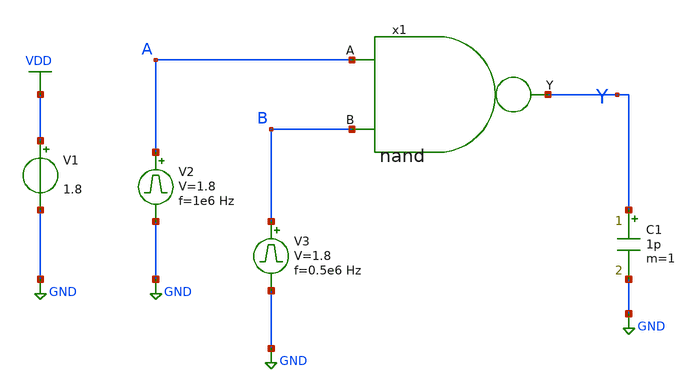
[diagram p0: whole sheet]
** sch_path: library/xschem/nand_tb.sch
**.subckt nand_tb
V1 VDD GND 1.8
V2 A GND pulse 0 1.8 '0.495/ 1e6 ' '0.01/1e6 ' '0.01/1e6 ' '0.49/1e6 ' '1/1e6 '
C1 Y GND 1p m=1
x1 A Y B nand
V3 B GND pulse 0 1.8 '0.495/ 0.5e6 ' '0.01/0.5e6 ' '0.01/0.5e6 ' '0.49/0.5e6 ' '1/0.5e6 '
**** begin user architecture code


.control
save all
tran 1n 2u
plot V(A) V(B)+2 V(Y)+4
.endc



** opencircuitdesign pdks install
.lib $::SKYWATER_MODELS/sky130.lib.spice tt


**** end user architecture code
**.ends

* expanding   symbol:  nand.sym # of pins=3
** sym_path: library/xschem/nand.sym
** sch_path: library/xschem/nand.sch
.subckt nand A Y B
*.ipin A
*.opin Y
*.ipin B
XM1 Y A net1 GND sky130_fd_pr__nfet_01v8 L=0.15 W=0.5 nf=1 ad='int((nf+1)/2) * W/nf * 0.29' as='int((nf+2)/2) * W/nf * 0.29'
+ pd='2*int((nf+1)/2) * (W/nf + 0.29)' ps='2*int((nf+2)/2) * (W/nf + 0.29)' nrd='0.29 / W' nrs='0.29 / W'
+ sa=0 sb=0 sd=0 mult=1 m=1
XM2 Y A VDD VDD sky130_fd_pr__pfet_01v8 L=0.15 W=1 nf=1 ad='int((nf+1)/2) * W/nf * 0.29' as='int((nf+2)/2) * W/nf * 0.29'
+ pd='2*int((nf+1)/2) * (W/nf + 0.29)' ps='2*int((nf+2)/2) * (W/nf + 0.29)' nrd='0.29 / W' nrs='0.29 / W'
+ sa=0 sb=0 sd=0 mult=1 m=1
XM3 Y B VDD VDD sky130_fd_pr__pfet_01v8 L=0.15 W=1 nf=1 ad='int((nf+1)/2) * W/nf * 0.29' as='int((nf+2)/2) * W/nf * 0.29'
+ pd='2*int((nf+1)/2) * (W/nf + 0.29)' ps='2*int((nf+2)/2) * (W/nf + 0.29)' nrd='0.29 / W' nrs='0.29 / W'
+ sa=0 sb=0 sd=0 mult=1 m=1
XM4 net1 B GND GND sky130_fd_pr__nfet_01v8 L=0.15 W=0.5 nf=1 ad='int((nf+1)/2) * W/nf * 0.29' as='int((nf+2)/2) * W/nf * 0.29'
+ pd='2*int((nf+1)/2) * (W/nf + 0.29)' ps='2*int((nf+2)/2) * (W/nf + 0.29)' nrd='0.29 / W' nrs='0.29 / W'
+ sa=0 sb=0 sd=0 mult=1 m=1
.ends

.GLOBAL VDD
.GLOBAL GND
.end
